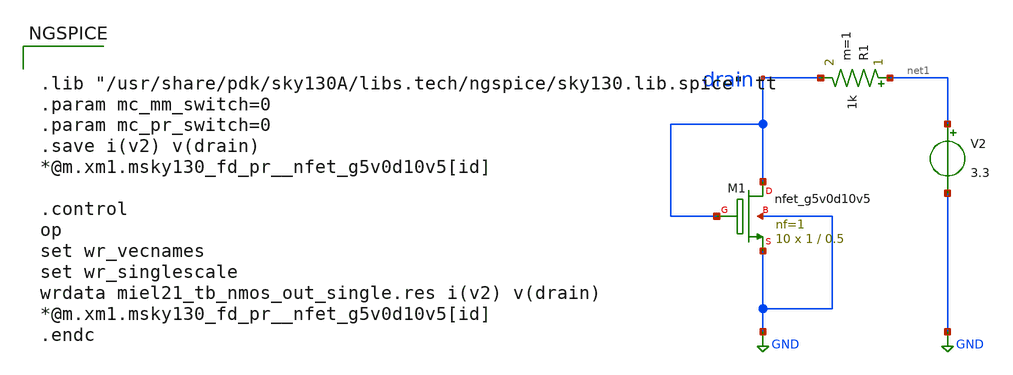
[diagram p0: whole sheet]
** sch_path: dev/opamp/miel21_tb_nmos_diode.sch
**.subckt miel21_tb_nmos_diode
V2 net1 GND 3.3
XM1 drain drain GND GND sky130_fd_pr__nfet_g5v0d10v5 L=0.5 W=1 nf=1 ad='int((nf+1)/2) * W/nf * 0.29'
+ as='int((nf+2)/2) * W/nf * 0.29' pd='2*int((nf+1)/2) * (W/nf + 0.29)' ps='2*int((nf+2)/2) * (W/nf + 0.29)'
+ nrd='0.29 / W' nrs='0.29 / W' sa=0 sb=0 sd=0 mult=10 m=10
R1 net1 drain 1k m=1
**** begin user architecture code


.lib "/usr/share/pdk/sky130A/libs.tech/ngspice/sky130.lib.spice" tt
.param mc_mm_switch=0
.param mc_pr_switch=0
.save i(v2) v(drain)
*@m.xm1.msky130_fd_pr__nfet_g5v0d10v5[id]

.control
op
set wr_vecnames
set wr_singlescale
wrdata miel21_tb_nmos_out_single.res i(v2) v(drain)
*@m.xm1.msky130_fd_pr__nfet_g5v0d10v5[id]
.endc


**** end user architecture code
**.ends
.GLOBAL GND
.end
